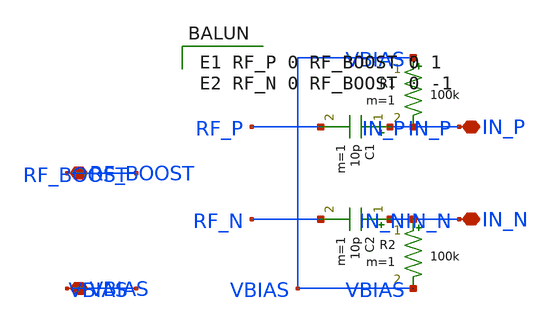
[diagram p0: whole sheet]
** sch_path: modules/PandaChip/designs/iris-harvester/splitter.sch
**.subckt splitter RF_BOOST VBIAS IN_P IN_N
*.iopin RF_BOOST
*.iopin VBIAS
*.iopin IN_P
*.iopin IN_N
C1 IN_P RF_P 10p m=1
C2 IN_N RF_N 10p m=1
R1 VBIAS IN_P 100k m=1
R2 IN_N VBIAS 100k m=1
**** begin user architecture code

E1 RF_P 0 RF_BOOST 0 1
E2 RF_N 0 RF_BOOST 0 -1

**** end user architecture code
**.ends
.end
